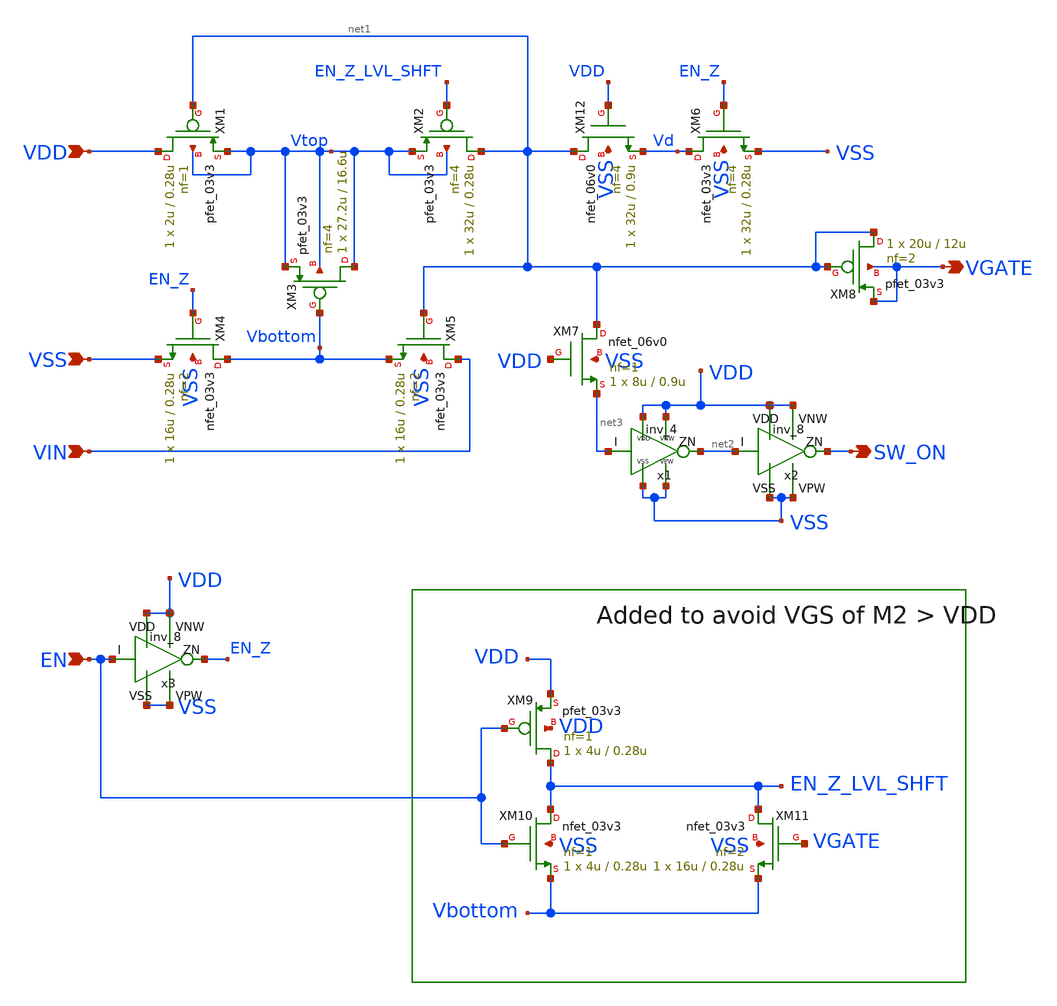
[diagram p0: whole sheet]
** sch_path: xschem/bootstrap.sch
**.subckt bootstrap VIN VSS VDD VGATE EN SW_ON
*.ipin VIN
*.ipin VSS
*.ipin VDD
*.opin VGATE
*.ipin EN
*.opin SW_ON
XM1 VDD net1 Vtop Vtop pfet_03v3 L=0.28u W=2u nf=1 ad='int((nf+1)/2) * W/nf * 0.18u' as='int((nf+2)/2) * W/nf * 0.18u'
+ pd='2*int((nf+1)/2) * (W/nf + 0.18u)' ps='2*int((nf+2)/2) * (W/nf + 0.18u)' nrd='0.18u / W' nrs='0.18u / W'
+ sa=0 sb=0 sd=0 m=1
XM2 net1 EN_Z_LVL_SHFT Vtop Vtop pfet_03v3 L=0.28u W=32u nf=4 ad='int((nf+1)/2) * W/nf * 0.18u' as='int((nf+2)/2) * W/nf * 0.18u'
+ pd='2*int((nf+1)/2) * (W/nf + 0.18u)' ps='2*int((nf+2)/2) * (W/nf + 0.18u)' nrd='0.18u / W' nrs='0.18u / W'
+ sa=0 sb=0 sd=0 m=1
XM3 Vtop Vbottom Vtop Vtop pfet_03v3 L=16.6u W=27.2u nf=4 ad='int((nf+1)/2) * W/nf * 0.18u' as='int((nf+2)/2) * W/nf * 0.18u'
+ pd='2*int((nf+1)/2) * (W/nf + 0.18u)' ps='2*int((nf+2)/2) * (W/nf + 0.18u)' nrd='0.18u / W' nrs='0.18u / W'
+ sa=0 sb=0 sd=0 m=1
XM4 Vbottom EN_Z VSS VSS nfet_03v3 L=0.28u W=16u nf=2 ad='int((nf+1)/2) * W/nf * 0.18u' as='int((nf+2)/2) * W/nf * 0.18u'
+ pd='2*int((nf+1)/2) * (W/nf + 0.18u)' ps='2*int((nf+2)/2) * (W/nf + 0.18u)' nrd='0.18u / W' nrs='0.18u / W'
+ sa=0 sb=0 sd=0 m=1
XM5 VIN net1 Vbottom VSS nfet_03v3 L=0.28u W=16u nf=2 ad='int((nf+1)/2) * W/nf * 0.18u' as='int((nf+2)/2) * W/nf * 0.18u'
+ pd='2*int((nf+1)/2) * (W/nf + 0.18u)' ps='2*int((nf+2)/2) * (W/nf + 0.18u)' nrd='0.18u / W' nrs='0.18u / W'
+ sa=0 sb=0 sd=0 m=1
XM6 Vd EN_Z VSS VSS nfet_03v3 L=0.28u W=32u nf=4 ad='int((nf+1)/2) * W/nf * 0.18u' as='int((nf+2)/2) * W/nf * 0.18u'
+ pd='2*int((nf+1)/2) * (W/nf + 0.18u)' ps='2*int((nf+2)/2) * (W/nf + 0.18u)' nrd='0.18u / W' nrs='0.18u / W'
+ sa=0 sb=0 sd=0 m=1
XM9 EN_Z_LVL_SHFT EN VDD VDD pfet_03v3 L=0.28u W=4u nf=1 ad='int((nf+1)/2) * W/nf * 0.18u' as='int((nf+2)/2) * W/nf * 0.18u'
+ pd='2*int((nf+1)/2) * (W/nf + 0.18u)' ps='2*int((nf+2)/2) * (W/nf + 0.18u)' nrd='0.18u / W' nrs='0.18u / W'
+ sa=0 sb=0 sd=0 m=1
XM10 EN_Z_LVL_SHFT EN Vbottom VSS nfet_03v3 L=0.28u W=4u nf=1 ad='int((nf+1)/2) * W/nf * 0.18u' as='int((nf+2)/2) * W/nf * 0.18u'
+ pd='2*int((nf+1)/2) * (W/nf + 0.18u)' ps='2*int((nf+2)/2) * (W/nf + 0.18u)' nrd='0.18u / W' nrs='0.18u / W'
+ sa=0 sb=0 sd=0 m=1
XM11 EN_Z_LVL_SHFT VGATE Vbottom VSS nfet_03v3 L=0.28u W=16u nf=2 ad='int((nf+1)/2) * W/nf * 0.18u' as='int((nf+2)/2) * W/nf * 0.18u'
+ pd='2*int((nf+1)/2) * (W/nf + 0.18u)' ps='2*int((nf+2)/2) * (W/nf + 0.18u)' nrd='0.18u / W' nrs='0.18u / W'
+ sa=0 sb=0 sd=0 m=1
XM12 net1 VDD Vd VSS nfet_06v0 L=0.9u W=32u nf=4 ad='int((nf+1)/2) * W/nf * 0.18u' as='int((nf+2)/2) * W/nf * 0.18u'
+ pd='2*int((nf+1)/2) * (W/nf + 0.18u)' ps='2*int((nf+2)/2) * (W/nf + 0.18u)' nrd='0.18u / W' nrs='0.18u / W'
+ sa=0 sb=0 sd=0 m=1
XM7 net1 VDD net3 VSS nfet_06v0 L=0.9u W=8u nf=1 ad='int((nf+1)/2) * W/nf * 0.18u' as='int((nf+2)/2) * W/nf * 0.18u'
+ pd='2*int((nf+1)/2) * (W/nf + 0.18u)' ps='2*int((nf+2)/2) * (W/nf + 0.18u)' nrd='0.18u / W' nrs='0.18u / W'
+ sa=0 sb=0 sd=0 m=1
XM8 net1 net1 VGATE VGATE pfet_03v3 L=12u W=20u nf=2 ad='int((nf+1)/2) * W/nf * 0.18u' as='int((nf+2)/2) * W/nf * 0.18u'
+ pd='2*int((nf+1)/2) * (W/nf + 0.18u)' ps='2*int((nf+2)/2) * (W/nf + 0.18u)' nrd='0.18u / W' nrs='0.18u / W'
+ sa=0 sb=0 sd=0 m=1
x2 net2 SW_ON VDD VDD VSS VSS gf180mcu_fd_sc_mcu7t5v0__inv_8
x3 EN EN_Z VDD VDD VSS VSS gf180mcu_fd_sc_mcu7t5v0__inv_8
x1 net3 net2 VDD VDD VSS VSS gf180mcu_fd_sc_mcu7t5v0__inv_4
**.ends
.end
